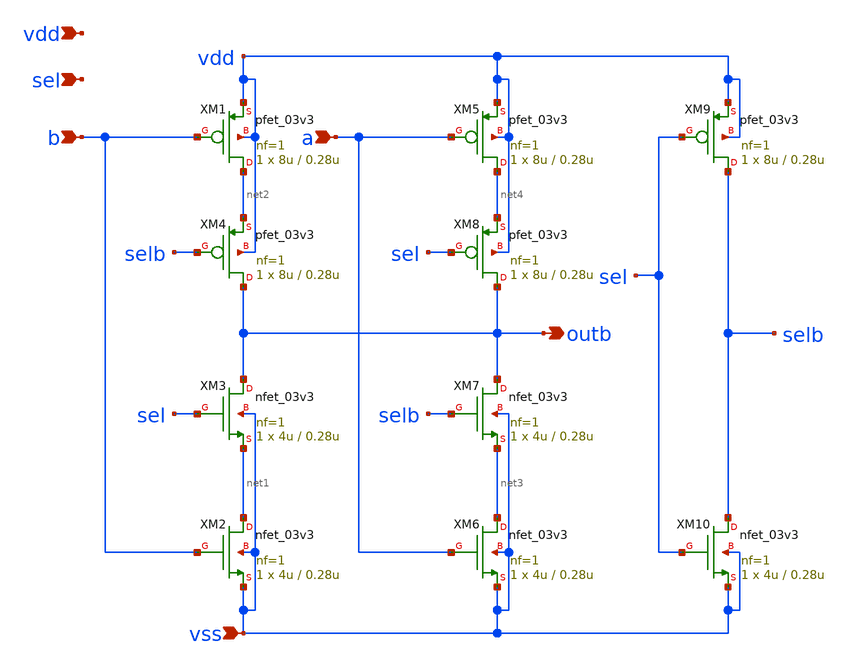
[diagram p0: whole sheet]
** sch_path: xschem/imux2.sch
**.subckt imux2 b a sel vdd vss outb
*.ipin b
*.ipin a
*.ipin sel
*.ipin vdd
*.ipin vss
*.opin outb
XM1 net2 b vdd vdd pfet_03v3 L=0.28u W=8u nf=1 ad='int((nf+1)/2) * W/nf * 0.18u' as='int((nf+2)/2) * W/nf * 0.18u'
+ pd='2*int((nf+1)/2) * (W/nf + 0.18u)' ps='2*int((nf+2)/2) * (W/nf + 0.18u)' nrd='0.18u / W' nrs='0.18u / W'
+ sa=0 sb=0 sd=0 m=1
XM2 net1 b vss vss nfet_03v3 L=0.28u W=4u nf=1 ad='int((nf+1)/2) * W/nf * 0.18u' as='int((nf+2)/2) * W/nf * 0.18u'
+ pd='2*int((nf+1)/2) * (W/nf + 0.18u)' ps='2*int((nf+2)/2) * (W/nf + 0.18u)' nrd='0.18u / W' nrs='0.18u / W'
+ sa=0 sb=0 sd=0 m=1
XM3 outb sel net1 vss nfet_03v3 L=0.28u W=4u nf=1 ad='int((nf+1)/2) * W/nf * 0.18u' as='int((nf+2)/2) * W/nf * 0.18u'
+ pd='2*int((nf+1)/2) * (W/nf + 0.18u)' ps='2*int((nf+2)/2) * (W/nf + 0.18u)' nrd='0.18u / W' nrs='0.18u / W'
+ sa=0 sb=0 sd=0 m=1
XM4 outb selb net2 vdd pfet_03v3 L=0.28u W=8u nf=1 ad='int((nf+1)/2) * W/nf * 0.18u' as='int((nf+2)/2) * W/nf * 0.18u'
+ pd='2*int((nf+1)/2) * (W/nf + 0.18u)' ps='2*int((nf+2)/2) * (W/nf + 0.18u)' nrd='0.18u / W' nrs='0.18u / W'
+ sa=0 sb=0 sd=0 m=1
XM5 net4 a vdd vdd pfet_03v3 L=0.28u W=8u nf=1 ad='int((nf+1)/2) * W/nf * 0.18u' as='int((nf+2)/2) * W/nf * 0.18u'
+ pd='2*int((nf+1)/2) * (W/nf + 0.18u)' ps='2*int((nf+2)/2) * (W/nf + 0.18u)' nrd='0.18u / W' nrs='0.18u / W'
+ sa=0 sb=0 sd=0 m=1
XM6 net3 a vss vss nfet_03v3 L=0.28u W=4u nf=1 ad='int((nf+1)/2) * W/nf * 0.18u' as='int((nf+2)/2) * W/nf * 0.18u'
+ pd='2*int((nf+1)/2) * (W/nf + 0.18u)' ps='2*int((nf+2)/2) * (W/nf + 0.18u)' nrd='0.18u / W' nrs='0.18u / W'
+ sa=0 sb=0 sd=0 m=1
XM7 outb selb net3 vss nfet_03v3 L=0.28u W=4u nf=1 ad='int((nf+1)/2) * W/nf * 0.18u' as='int((nf+2)/2) * W/nf * 0.18u'
+ pd='2*int((nf+1)/2) * (W/nf + 0.18u)' ps='2*int((nf+2)/2) * (W/nf + 0.18u)' nrd='0.18u / W' nrs='0.18u / W'
+ sa=0 sb=0 sd=0 m=1
XM8 outb sel net4 vdd pfet_03v3 L=0.28u W=8u nf=1 ad='int((nf+1)/2) * W/nf * 0.18u' as='int((nf+2)/2) * W/nf * 0.18u'
+ pd='2*int((nf+1)/2) * (W/nf + 0.18u)' ps='2*int((nf+2)/2) * (W/nf + 0.18u)' nrd='0.18u / W' nrs='0.18u / W'
+ sa=0 sb=0 sd=0 m=1
XM9 selb sel vdd vdd pfet_03v3 L=0.28u W=8u nf=1 ad='int((nf+1)/2) * W/nf * 0.18u' as='int((nf+2)/2) * W/nf * 0.18u'
+ pd='2*int((nf+1)/2) * (W/nf + 0.18u)' ps='2*int((nf+2)/2) * (W/nf + 0.18u)' nrd='0.18u / W' nrs='0.18u / W'
+ sa=0 sb=0 sd=0 m=1
XM10 selb sel vss vss nfet_03v3 L=0.28u W=4u nf=1 ad='int((nf+1)/2) * W/nf * 0.18u' as='int((nf+2)/2) * W/nf * 0.18u'
+ pd='2*int((nf+1)/2) * (W/nf + 0.18u)' ps='2*int((nf+2)/2) * (W/nf + 0.18u)' nrd='0.18u / W' nrs='0.18u / W'
+ sa=0 sb=0 sd=0 m=1
**.ends
.end
